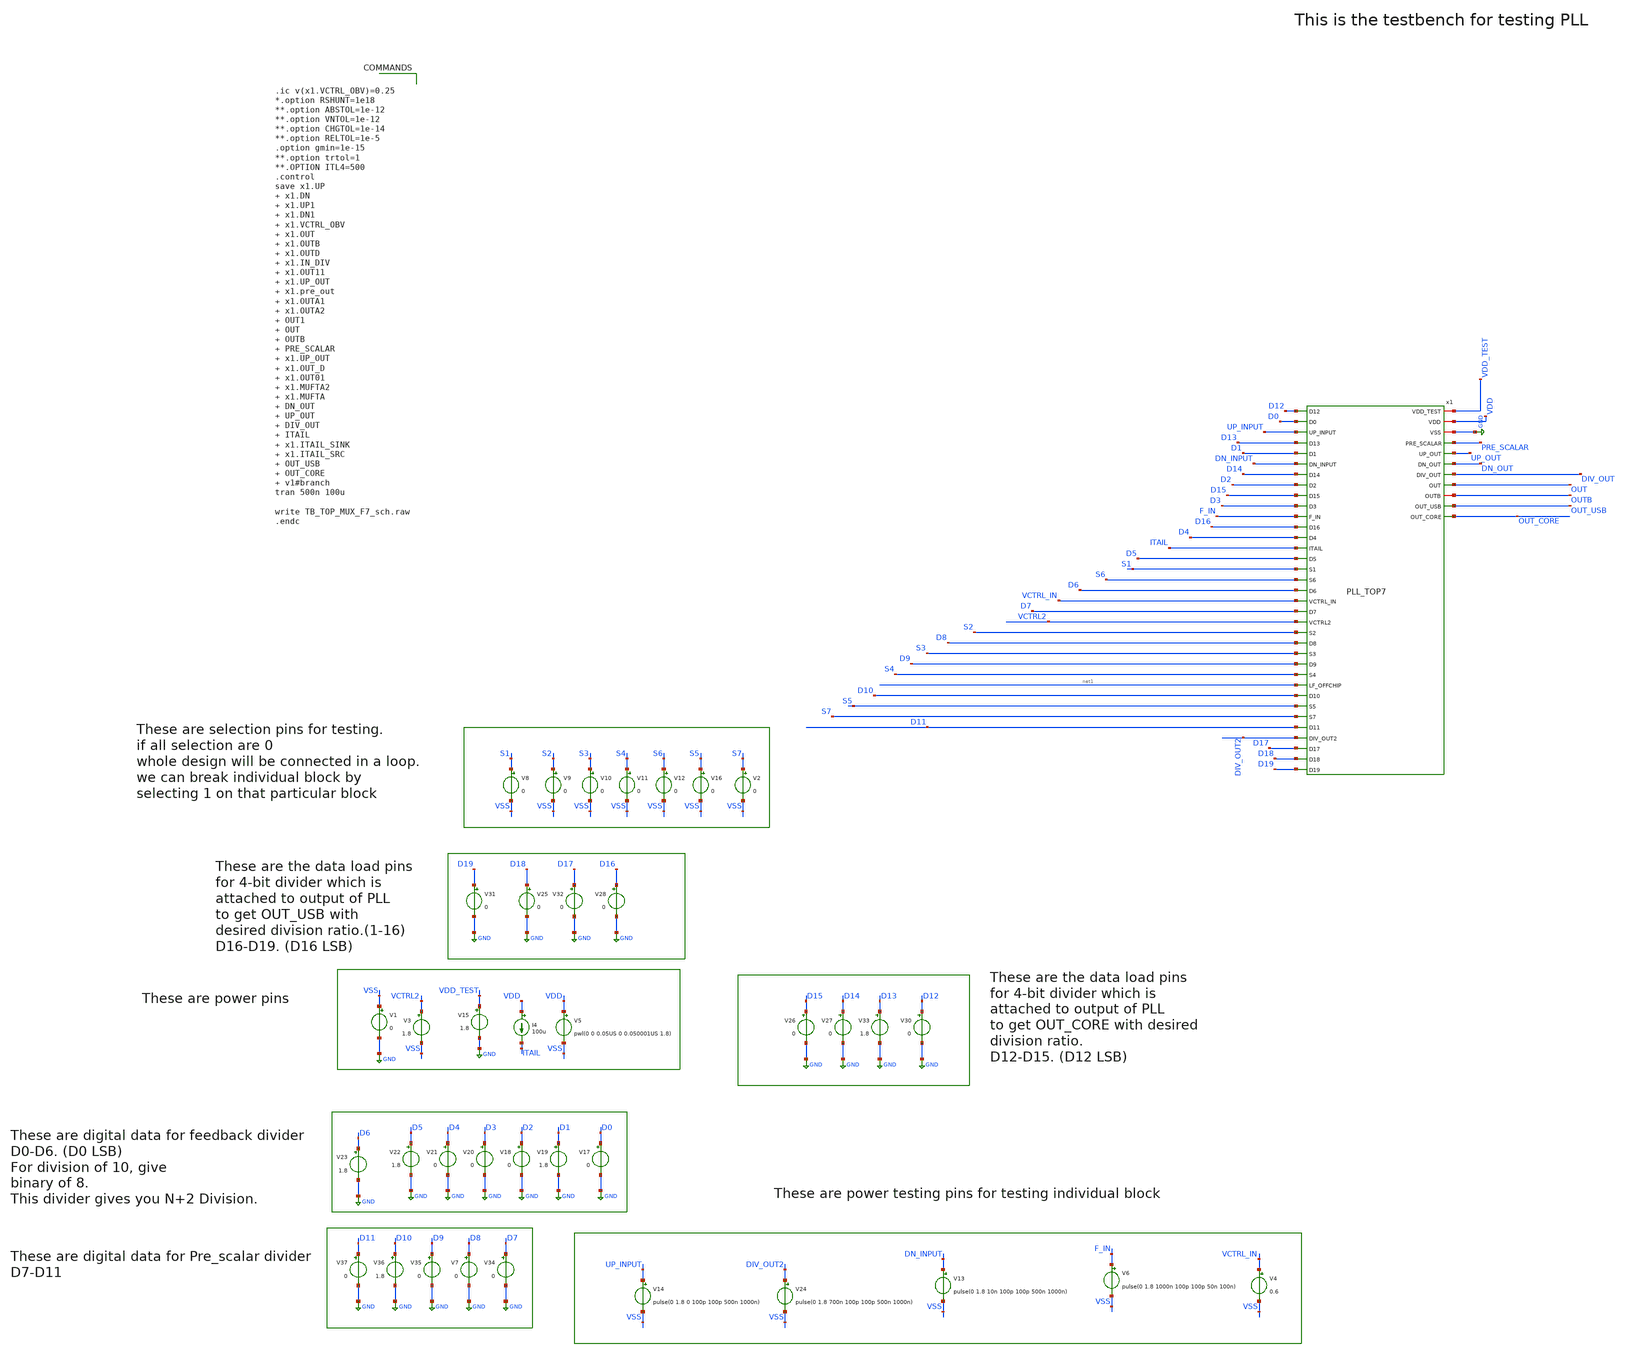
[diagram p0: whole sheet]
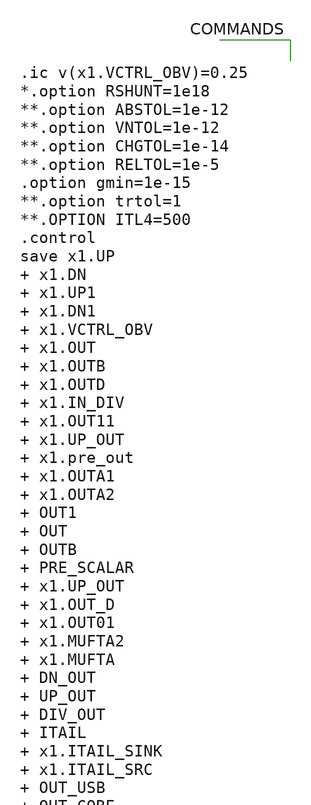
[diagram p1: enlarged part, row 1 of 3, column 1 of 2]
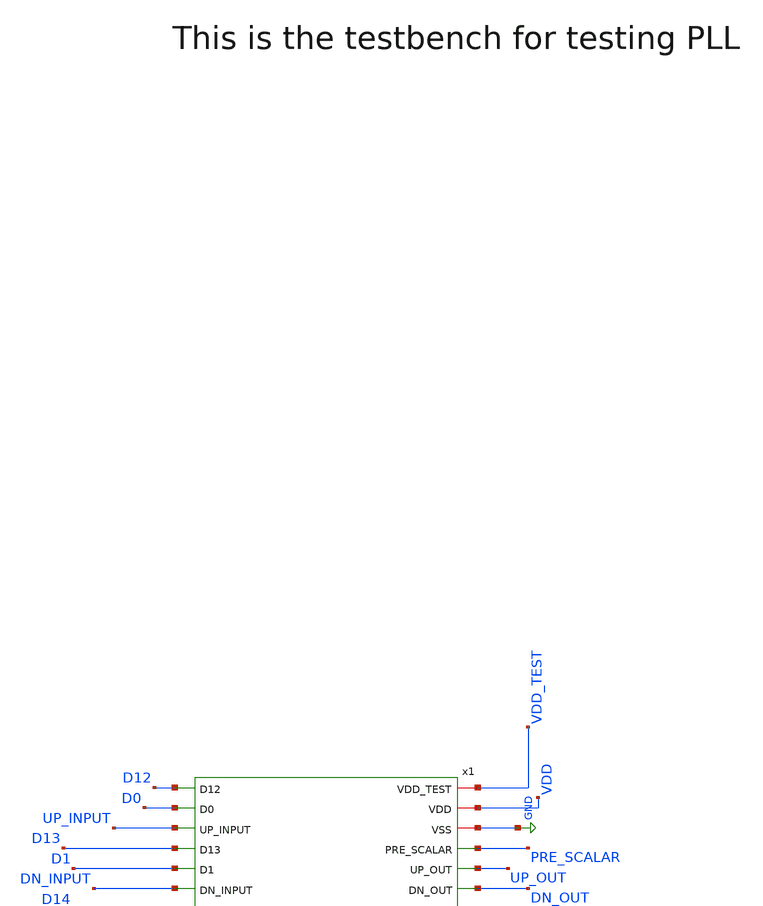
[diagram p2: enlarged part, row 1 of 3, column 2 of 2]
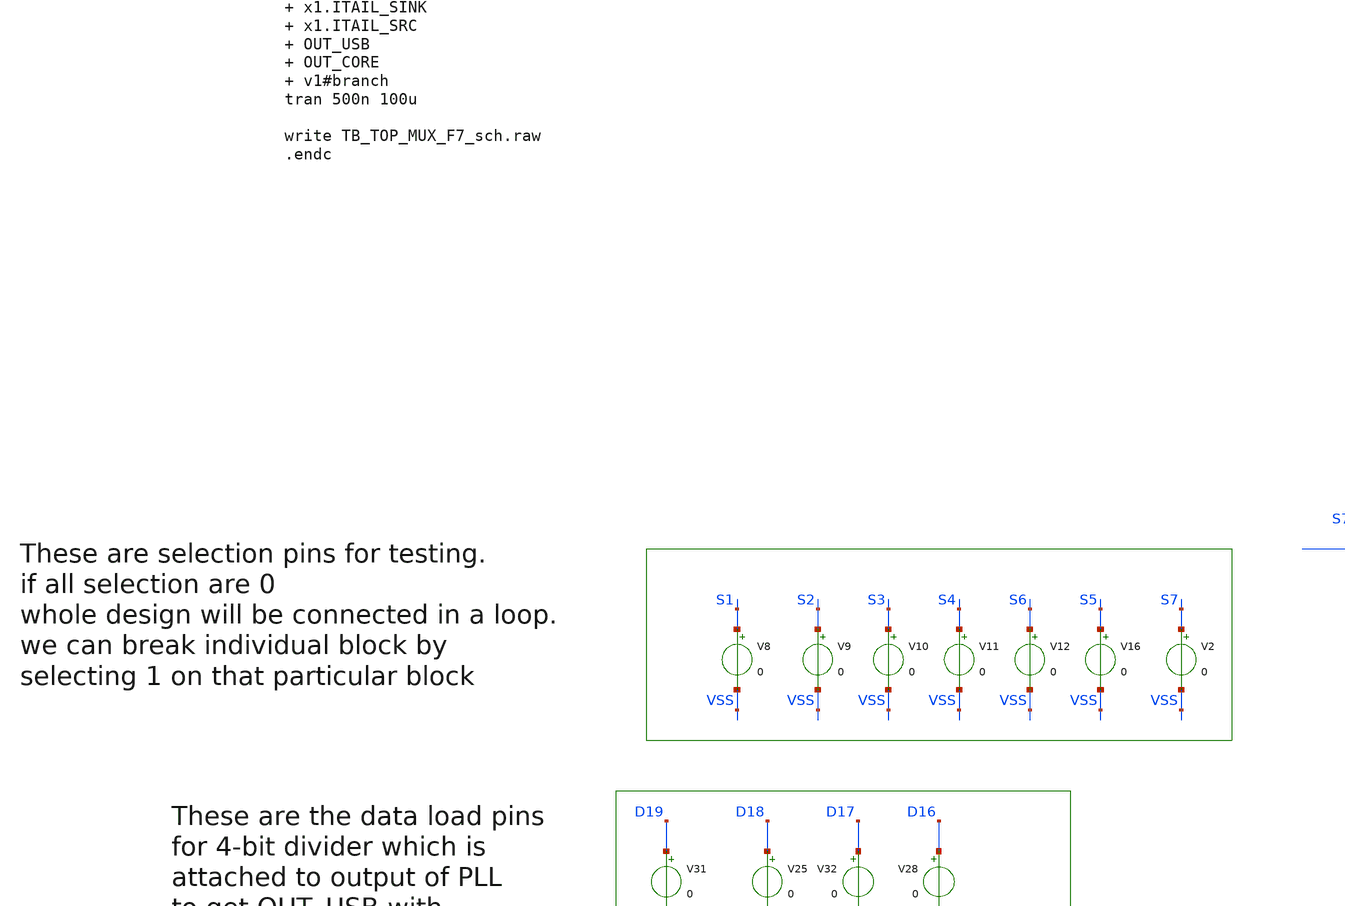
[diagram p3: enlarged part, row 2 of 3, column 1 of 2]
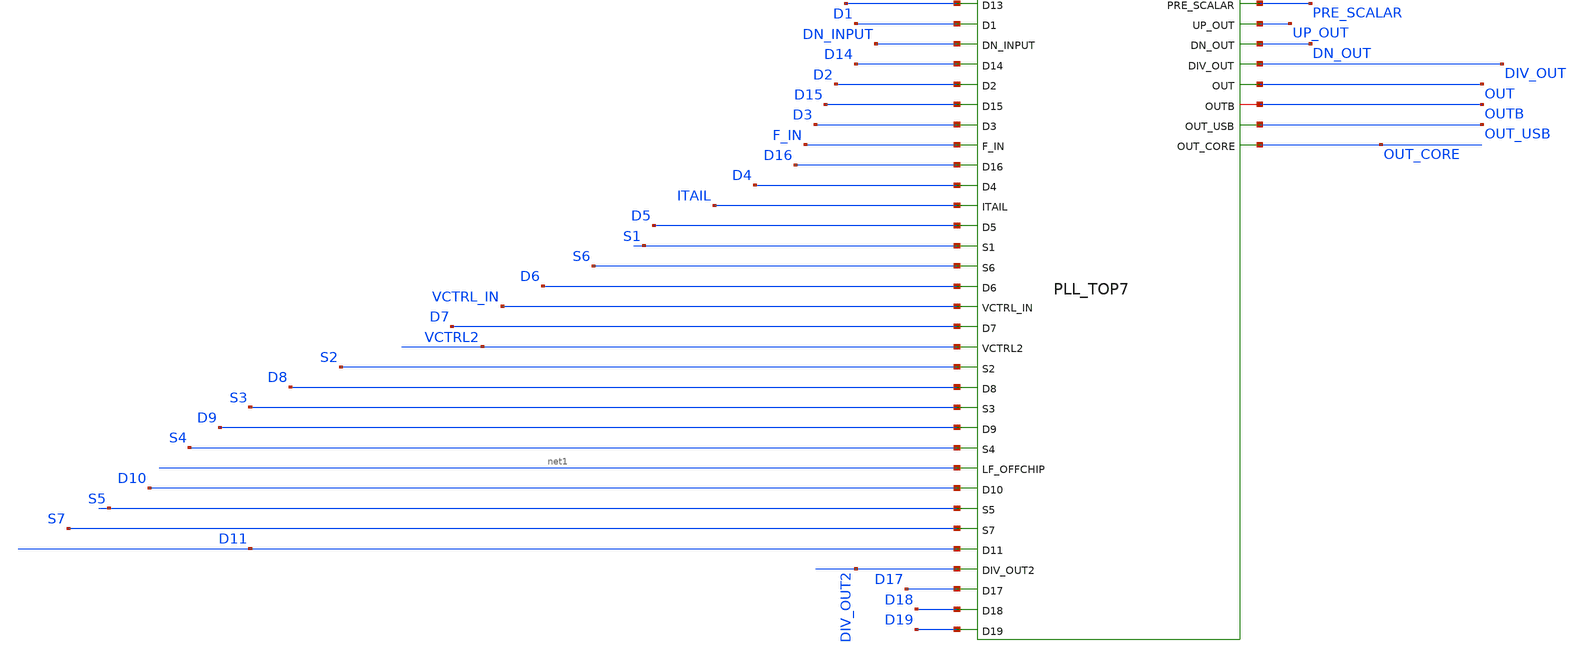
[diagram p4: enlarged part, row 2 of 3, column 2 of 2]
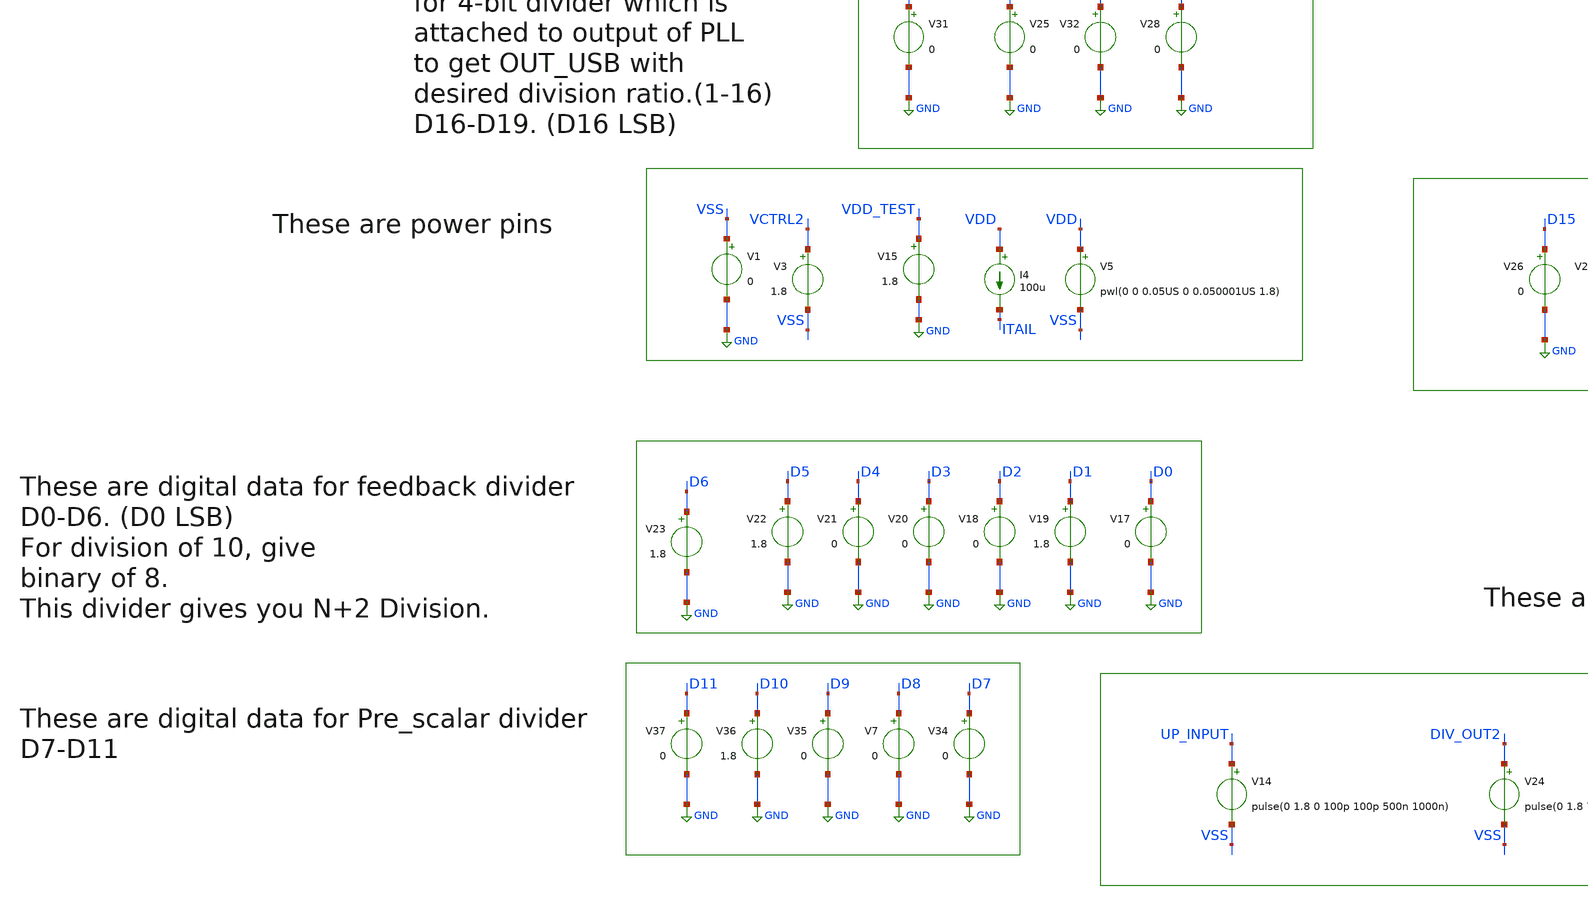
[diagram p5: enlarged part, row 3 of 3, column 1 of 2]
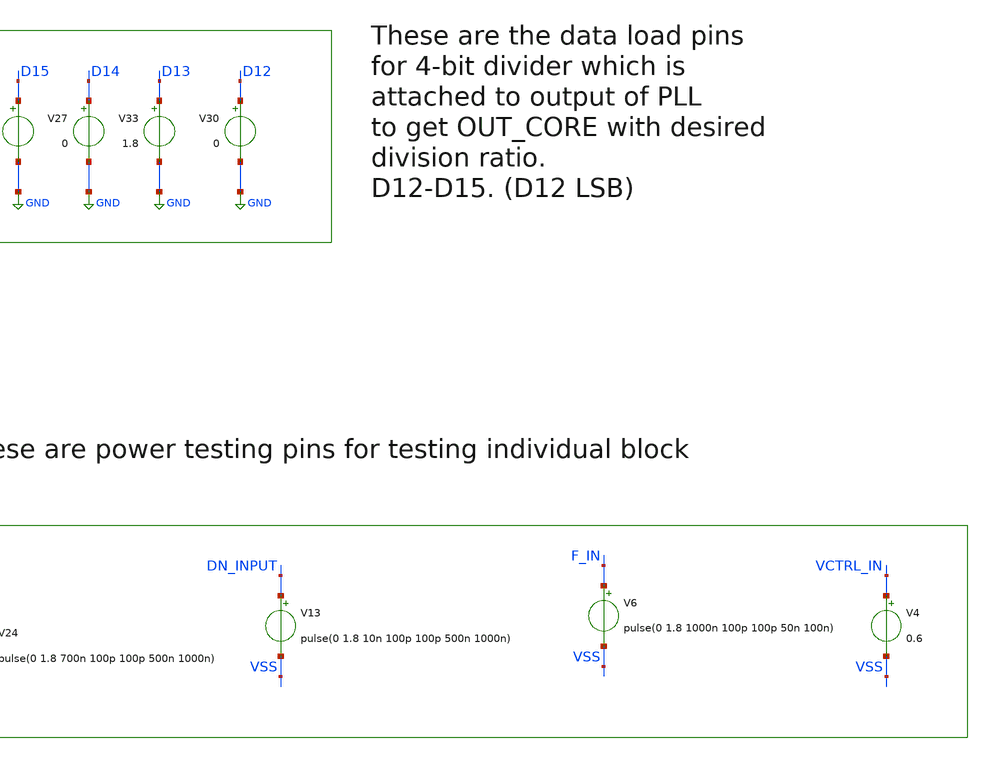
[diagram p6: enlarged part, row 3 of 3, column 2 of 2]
** sch_path: xschem/TB_TOP_MUX_F7_sch.sch
**.subckt TB_TOP_MUX_F7_sch
V1 VSS GND 0
V4 VCTRL_IN VSS 0.6
V6 F_IN VSS pulse(0 1.8 1000n 100p 100p 50n 100n)
I4 VDD ITAIL 100u
V8 S1 VSS 0
V9 S2 VSS 0
V10 S3 VSS 0
V11 S4 VSS 0
V12 S6 VSS 0
V13 DN_INPUT VSS pulse(0 1.8 10n 100p 100p 500n 1000n)
V14 UP_INPUT VSS pulse(0 1.8 0 100p 100p 500n 1000n)
V16 S5 VSS 0
V17 D0 GND 0
V2 S7 VSS 0
V5 VDD VSS pwl(0 0 0.05US 0 0.050001US 1.8)
V35 D9 GND 0
V37 D11 GND 0
V24 DIV_OUT2 VSS pulse(0 1.8 700n 100p 100p 500n 1000n)
V20 D3 GND 0
V22 D5 GND 1.8
V3 VCTRL2 VSS 1.8
V15 VDD_TEST GND 1.8
V36 D10 GND 1.8
V7 D8 GND 0
V34 D7 GND 0
V21 D4 GND 0
V23 D6 GND 1.8
V25 D18 GND 0
V26 D15 GND 0
V31 D19 GND 0
V28 D16 GND 0
V27 D14 GND 0
V30 D12 GND 0
V32 D17 GND 0
V18 D2 GND 0
V19 D1 GND 1.8
V33 D13 GND 1.8
x1 VDD_TEST D12 D0 VDD UP_INPUT D13 D1 DN_INPUT GND D14 D2 PRE_SCALAR UP_OUT D15 D3 F_IN DN_OUT D16
+ D4 ITAIL DIV_OUT D5 S1 S6 D6 VCTRL_IN D7 VCTRL2 S2 D8 S3 OUT D9 OUTB S4 net1 D10 S5 S7 D11 OUT_USB
+ DIV_OUT2 D17 OUT_CORE D18 D19 PLL_TOP7
**** begin user architecture code


.ic v(x1.VCTRL_OBV)=0.25
*.option RSHUNT=1e18
**.option ABSTOL=1e-12
**.option VNTOL=1e-12
**.option CHGTOL=1e-14
**.option RELTOL=1e-5
.option gmin=1e-15
**.option trtol=1
**.OPTION ITL4=500
.control
save x1.UP  x1.DN  x1.UP1  x1.DN1  x1.VCTRL_OBV  x1.OUT  x1.OUTB  x1.OUTD  x1.IN_DIV  x1.OUT11
+  x1.UP_OUT  x1.pre_out  x1.OUTA1  x1.OUTA2  OUT1  OUT  OUTB  PRE_SCALAR  x1.UP_OUT  x1.OUT_D  x1.OUT01
+  x1.MUFTA2  x1.MUFTA  DN_OUT  UP_OUT  DIV_OUT  ITAIL  x1.ITAIL_SINK  x1.ITAIL_SRC  OUT_USB  OUT_CORE
+  v1#branch
tran 500n 100u

write TB_TOP_MUX_F7_sch.raw
.endc



** opencircuitdesign pdks install
.lib $::SKYWATER_MODELS/sky130.lib.spice tt


**** end user architecture code
**.ends
.GLOBAL GND
.end
